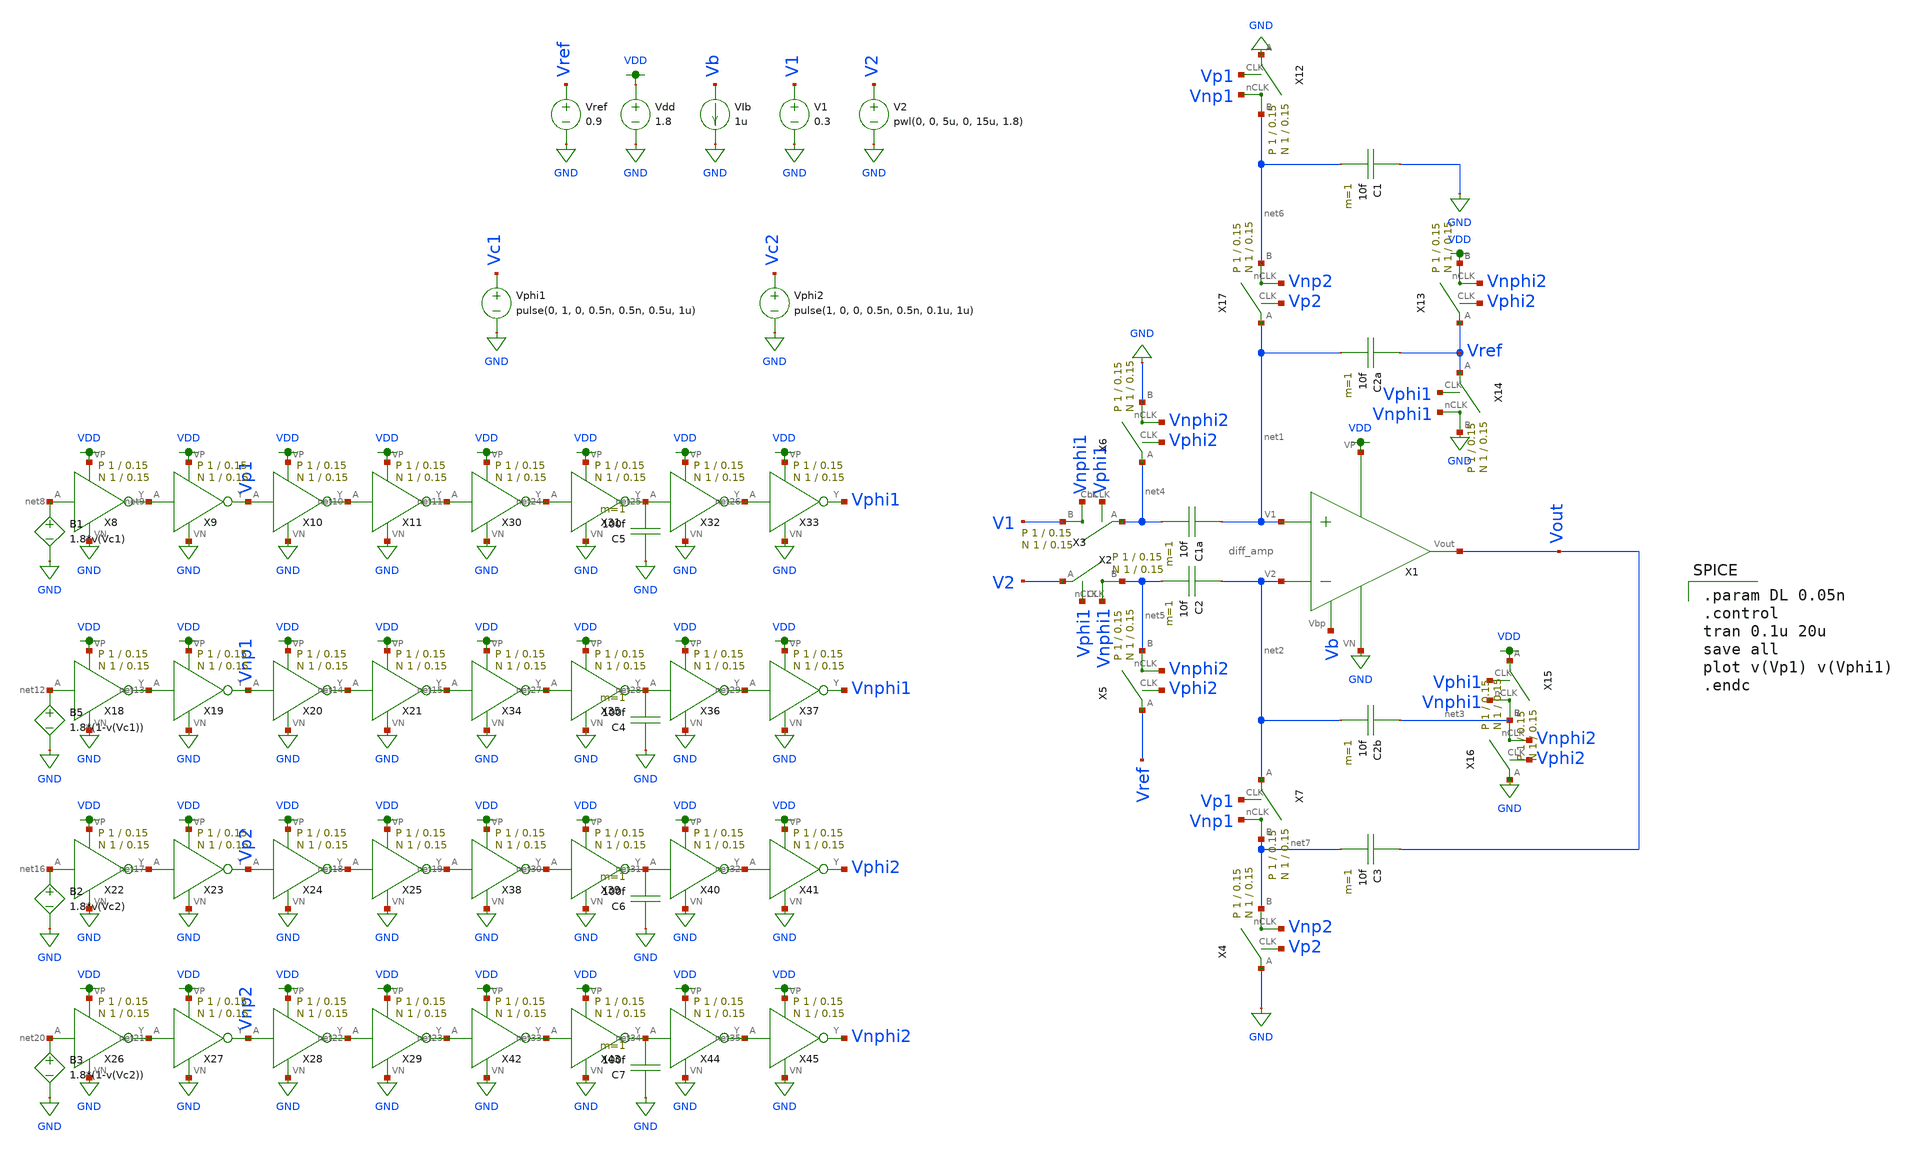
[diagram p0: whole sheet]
** sch_path: schematic/test/alpha_amp_differentialGE.sch
**.subckt alpha_amp_differentialGE
X1 VDD Vb Vout net1 net2 GND diff_amp
C1a net1 net4 10f m=1
C2 net2 net5 10f m=1
C2a Vref net1 10f m=1
C2b net3 net2 10f m=1
X2 V1 net4 Vphi1 Vnphi1 switch Wp=1 Lp=0.15 WW=1 LL=0.15
X3 net5 V2 Vphi1 Vnphi1 switch Wp=1 Lp=0.15 WW=1 LL=0.15
X4 net7 GND Vp2 Vnp2 switch Wp=1 Lp=0.15 WW=1 LL=0.15
X5 net5 Vref Vphi2 Vnphi2 switch Wp=1 Lp=0.15 WW=1 LL=0.15
X7 net7 net2 Vp1 Vnp1 switch Wp=1 Lp=0.15 WW=1 LL=0.15
Vdd VDD GND 1.8
V1 V1 GND 0.3
V2 V2 GND pwl(0, 0, 5u, 0, 15u, 1.8)
Vphi1 Vc1 GND pulse(0, 1, 0, 0.5n, 0.5n, 0.5u, 1u)
VIb Vb GND 1u
Vphi2 Vc2 GND pulse(1, 0, 0, 0.5n, 0.5n, 0.1u, 1u)
Vref Vref GND 0.9
X12 net6 GND Vp1 Vnp1 switch Wp=1 Lp=0.15 WW=1 LL=0.15
X13 VDD Vref Vphi2 Vnphi2 switch Wp=1 Lp=0.15 WW=1 LL=0.15
X6 GND net4 Vphi2 Vnphi2 switch Wp=1 Lp=0.15 WW=1 LL=0.15
C1 GND net6 10f m=1
X14 GND Vref Vphi1 Vnphi1 switch Wp=1 Lp=0.15 WW=1 LL=0.15
X15 net3 VDD Vphi1 Vnphi1 switch Wp=1 Lp=0.15 WW=1 LL=0.15
X16 net3 GND Vphi2 Vnphi2 switch Wp=1 Lp=0.15 WW=1 LL=0.15
C3 Vout net7 10f m=1
X17 net6 net1 Vp2 Vnp2 switch Wp=1 Lp=0.15 WW=1 LL=0.15
B1 net8 GND V=1.8*v(Vc1)
X8 net8 net9 VDD GND inverter Wp=1 Lp=0.15 WW=1 LL=0.15
X9 net9 Vp1 VDD GND inverter Wp=1 Lp=0.15 WW=1 LL=0.15
X10 Vp1 net10 VDD GND inverter Wp=1 Lp=0.15 WW=1 LL=0.15
X11 net10 net11 VDD GND inverter Wp=1 Lp=0.15 WW=1 LL=0.15
B5 net12 GND V=1.8*(1-v(Vc1))
X18 net12 net13 VDD GND inverter Wp=1 Lp=0.15 WW=1 LL=0.15
X19 net13 Vnp1 VDD GND inverter Wp=1 Lp=0.15 WW=1 LL=0.15
X20 Vnp1 net14 VDD GND inverter Wp=1 Lp=0.15 WW=1 LL=0.15
X21 net14 net15 VDD GND inverter Wp=1 Lp=0.15 WW=1 LL=0.15
B2 net16 GND V=1.8*v(Vc2)
X22 net16 net17 VDD GND inverter Wp=1 Lp=0.15 WW=1 LL=0.15
X23 net17 Vp2 VDD GND inverter Wp=1 Lp=0.15 WW=1 LL=0.15
X24 Vp2 net18 VDD GND inverter Wp=1 Lp=0.15 WW=1 LL=0.15
X25 net18 net19 VDD GND inverter Wp=1 Lp=0.15 WW=1 LL=0.15
B3 net20 GND V=1.8*(1-v(Vc2))
X26 net20 net21 VDD GND inverter Wp=1 Lp=0.15 WW=1 LL=0.15
X27 net21 Vnp2 VDD GND inverter Wp=1 Lp=0.15 WW=1 LL=0.15
X28 Vnp2 net22 VDD GND inverter Wp=1 Lp=0.15 WW=1 LL=0.15
X29 net22 net23 VDD GND inverter Wp=1 Lp=0.15 WW=1 LL=0.15
X30 net11 net24 VDD GND inverter Wp=1 Lp=0.15 WW=1 LL=0.15
X31 net24 net25 VDD GND inverter Wp=1 Lp=0.15 WW=1 LL=0.15
X32 net25 net26 VDD GND inverter Wp=1 Lp=0.15 WW=1 LL=0.15
X33 net26 Vphi1 VDD GND inverter Wp=1 Lp=0.15 WW=1 LL=0.15
X34 net15 net27 VDD GND inverter Wp=1 Lp=0.15 WW=1 LL=0.15
X35 net27 net28 VDD GND inverter Wp=1 Lp=0.15 WW=1 LL=0.15
X36 net28 net29 VDD GND inverter Wp=1 Lp=0.15 WW=1 LL=0.15
X37 net29 Vnphi1 VDD GND inverter Wp=1 Lp=0.15 WW=1 LL=0.15
X38 net19 net30 VDD GND inverter Wp=1 Lp=0.15 WW=1 LL=0.15
X39 net30 net31 VDD GND inverter Wp=1 Lp=0.15 WW=1 LL=0.15
X40 net31 net32 VDD GND inverter Wp=1 Lp=0.15 WW=1 LL=0.15
X41 net32 Vphi2 VDD GND inverter Wp=1 Lp=0.15 WW=1 LL=0.15
X42 net23 net33 VDD GND inverter Wp=1 Lp=0.15 WW=1 LL=0.15
X43 net33 net34 VDD GND inverter Wp=1 Lp=0.15 WW=1 LL=0.15
X44 net34 net35 VDD GND inverter Wp=1 Lp=0.15 WW=1 LL=0.15
X45 net35 Vnphi2 VDD GND inverter Wp=1 Lp=0.15 WW=1 LL=0.15
C4 GND net28 100f m=1
C5 GND net25 100f m=1
C6 GND net31 100f m=1
C7 GND net34 100f m=1
**** begin user architecture code

.option wnflag=1
.param MC_SWITCH=0.0
.lib ~/skywater/skywater-pdk/libraries/sky130_fd_pr_ngspice/latest/models/sky130.lib.spice tt


.param DL 0.05n
.control
tran 0.1u 20u
save all
plot v(Vp1) v(Vphi1)
.endc

**** end user architecture code
**.ends
.GLOBAL GND
.GLOBAL VDD
.end
